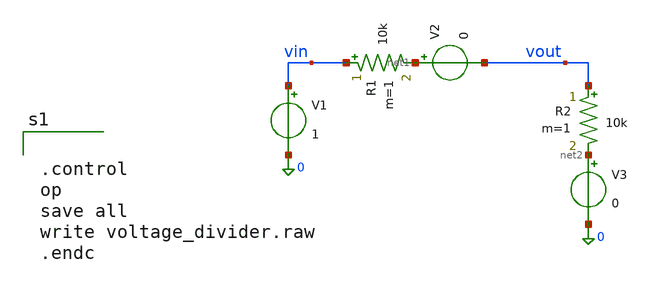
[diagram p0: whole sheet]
** sch_path: mag/layout/voltage_divider.sch
**.subckt voltage_divider
V1 vin 0 1
R1 vin net1 10k m=1
R2 vout net2 10k m=1
V2 net1 vout 0
V3 net2 0 0
**** begin user architecture code


.control
op
save all
write voltage_divider.raw
.endc

**** end user architecture code
**.ends
.end
